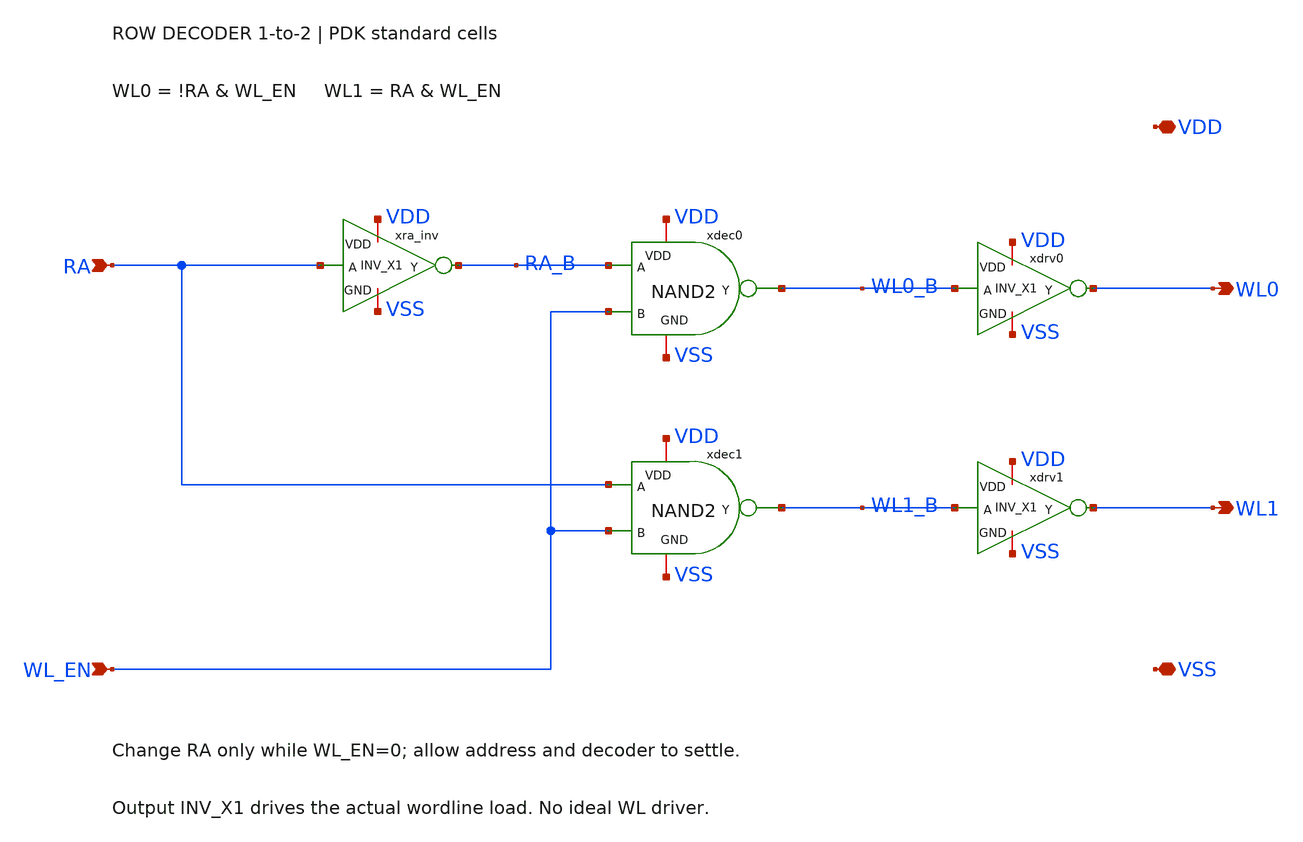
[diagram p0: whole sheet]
** sch_path: member_project/SRAM/PenguinEino/learning/schematics/row_decoder_1to2.sch
**.subckt row_decoder_1to2 RA WL_EN WL0 WL1 VDD VSS
*.ipin RA
*.ipin WL_EN
*.opin WL0
*.opin WL1
*.iopin VDD
*.iopin VSS
xra_inv VDD RA RA_B VSS INV_X1
xdec0 VDD WL0_B RA_B WL_EN VSS NAND2
xdrv0 VDD WL0_B WL0 VSS INV_X1
xdec1 VDD WL1_B RA WL_EN VSS NAND2
xdrv1 VDD WL1_B WL1 VSS INV_X1
**.ends
.end
